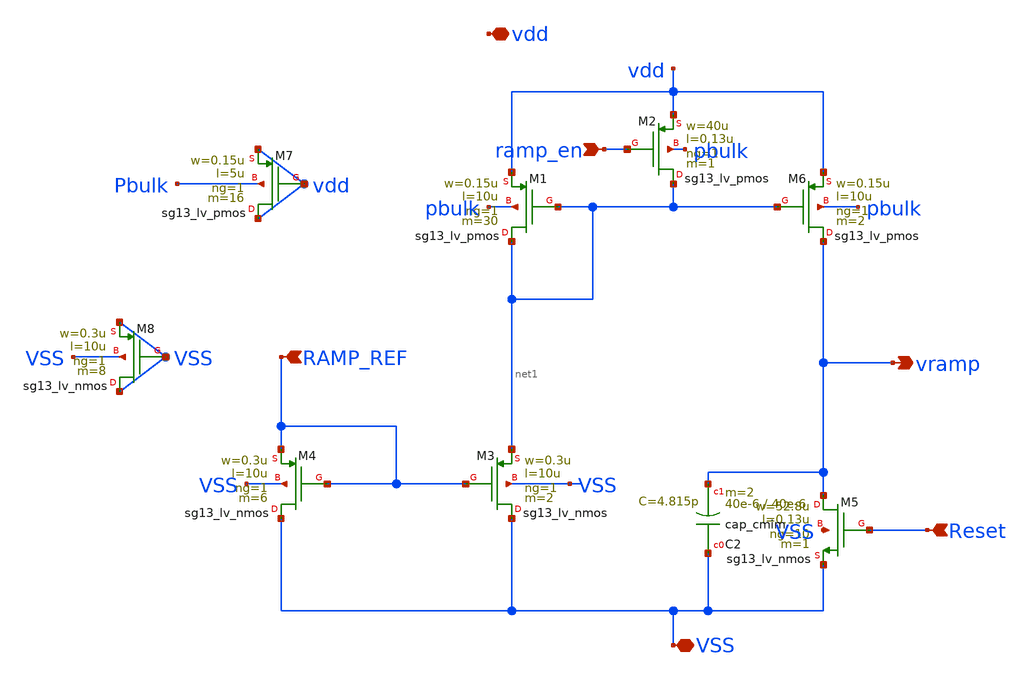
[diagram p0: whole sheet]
** sch_path: dependencies/ADC/dependencies/RAMP_GEN/RAMP_GEN-main/schematic/xschem/ramp_generator.sch
**.subckt ramp_generator ramp_en VSS vdd Reset vramp RAMP_REF
*.ipin ramp_en
*.iopin VSS
*.iopin vdd
*.ipin Reset
*.opin vramp
*.ipin RAMP_REF
XM5 vramp Reset VSS VSS sg13_lv_nmos w=52.8u l=0.13u ng=10 m=1 mm_ok=1
XM6 vramp net1 vdd pbulk sg13_lv_pmos w=0.15u l=10u ng=1 m=2 mm_ok=1
XM1 net1 net1 vdd pbulk sg13_lv_pmos w=0.15u l=10u ng=1 m=30 mm_ok=1
XM2 net1 ramp_en vdd pbulk sg13_lv_pmos w=40u l=0.13u ng=1 m=1 mm_ok=1
XM3 VSS RAMP_REF net1 VSS sg13_lv_nmos w=0.3u l=10u ng=1 m=2 mm_ok=1
XM4 VSS RAMP_REF RAMP_REF VSS sg13_lv_nmos w=0.3u l=10u ng=1 m=6 mm_ok=1
XC2 VSS vramp cap_cmim w=40e-6 l=40e-6 m=2 mm_ok=1
XM7 vdd vdd vdd Pbulk sg13_lv_pmos w=0.15u l=5u ng=1 m=16 mm_ok=1
XM8 VSS VSS VSS VSS sg13_lv_nmos w=0.3u l=10u ng=1 m=8 mm_ok=1
**.ends
.end
